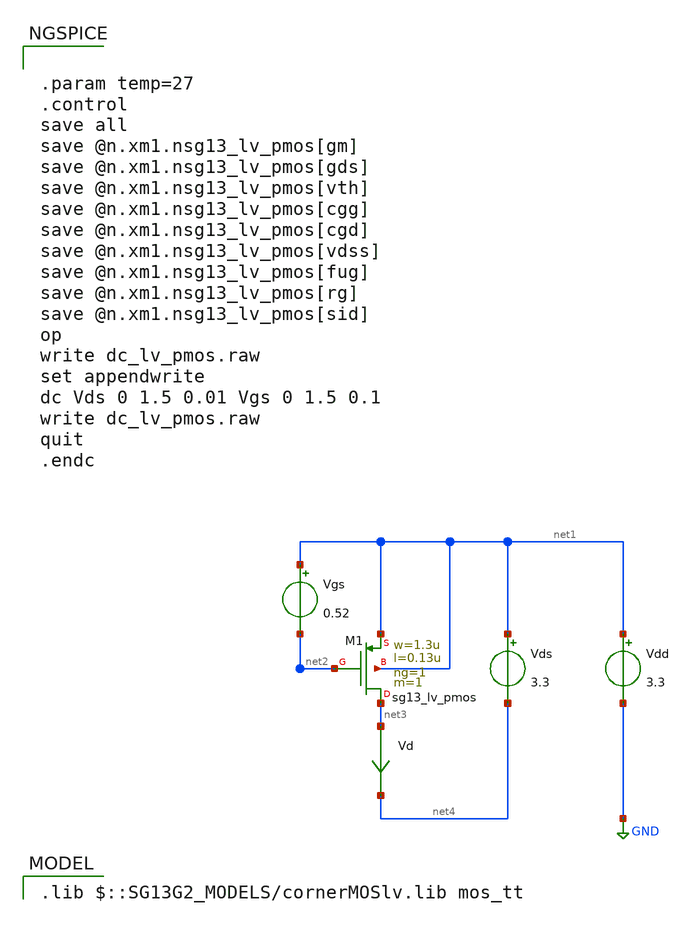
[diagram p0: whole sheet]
** sch_path: xschem/dc_lv_pmos.sch
* Copyright 2023-2024 IHP PDK Authors, Harald Pretl
**.subckt dc_lv_pmos
Vgs net1 net2 0.52
Vds net1 net4 3.3
Vd net3 net4 0
.save i(vd)
XM1 net3 net2 net1 net1 sg13_lv_pmos w=1.3u l=0.13u ng=1 m=1 mm_ok=1
Vdd net1 GND 3.3
**** begin user architecture code
 .lib $::SG13G2_MODELS/cornerMOSlv.lib mos_tt



.param temp=27
.control
save all
save @n.xm1.nsg13_lv_pmos[gm]
save @n.xm1.nsg13_lv_pmos[gds]
save @n.xm1.nsg13_lv_pmos[vth]
save @n.xm1.nsg13_lv_pmos[cgg]
save @n.xm1.nsg13_lv_pmos[cgd]
save @n.xm1.nsg13_lv_pmos[vdss]
save @n.xm1.nsg13_lv_pmos[fug]
save @n.xm1.nsg13_lv_pmos[rg]
save @n.xm1.nsg13_lv_pmos[sid]
op
write dc_lv_pmos.raw
set appendwrite
dc Vds 0 1.5 0.01 Vgs 0 1.5 0.1
write dc_lv_pmos.raw
quit
.endc


**** end user architecture code
**.ends
.GLOBAL GND
.end
